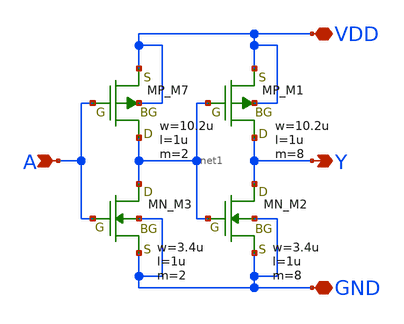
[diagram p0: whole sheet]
** sch_path: libs.tech/xschem/TR-1um_stdcell/BUF_X8.sch
**.subckt BUF_X8 A Y VDD GND
*.ipin A
*.opin Y
*.iopin VDD
*.iopin GND
XM7 net1 A VDD VDD PMOS w=10.2u l=1u nrd=0 nrs=0 m=2
XM1 Y net1 VDD VDD PMOS w=10.2u l=1u nrd=0 nrs=0 m=8
XM3 net1 A GND GND NMOS w=3.4u l=1u nrd=0 nrs=0 m=2
XM2 Y net1 GND GND NMOS w=3.4u l=1u nrd=0 nrs=0 m=8
**.ends
.end
